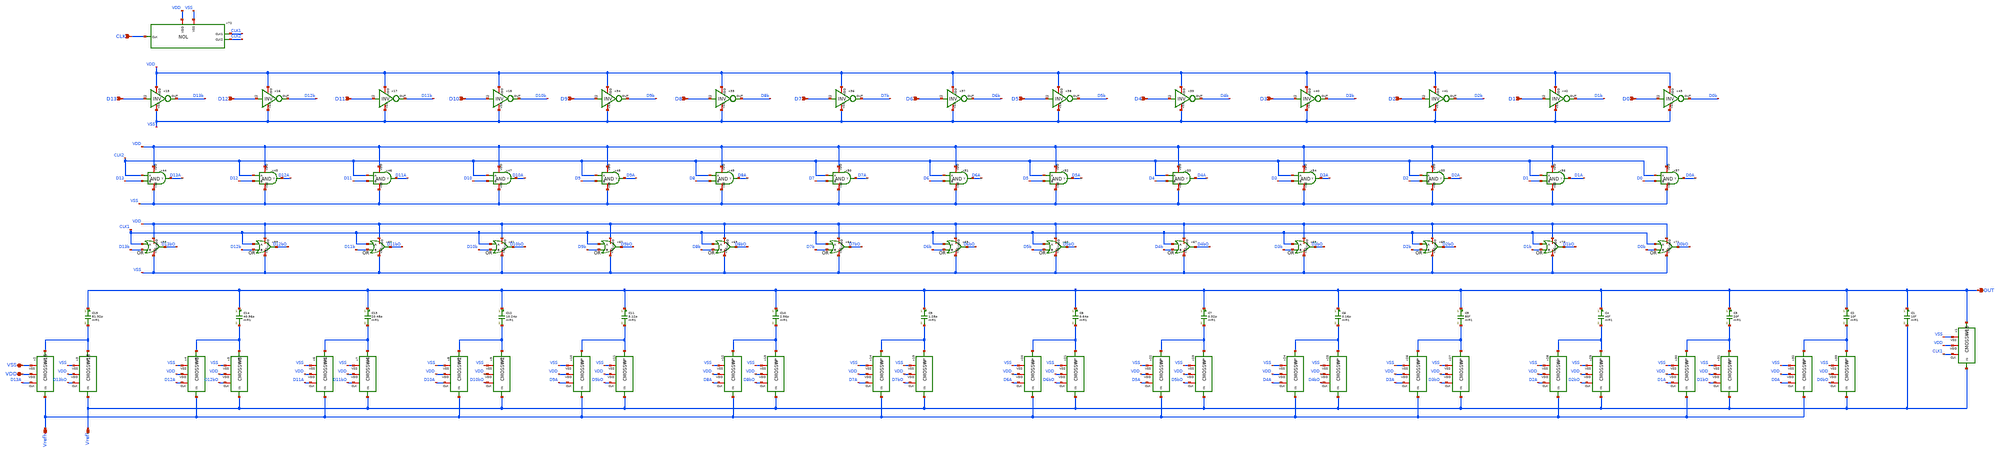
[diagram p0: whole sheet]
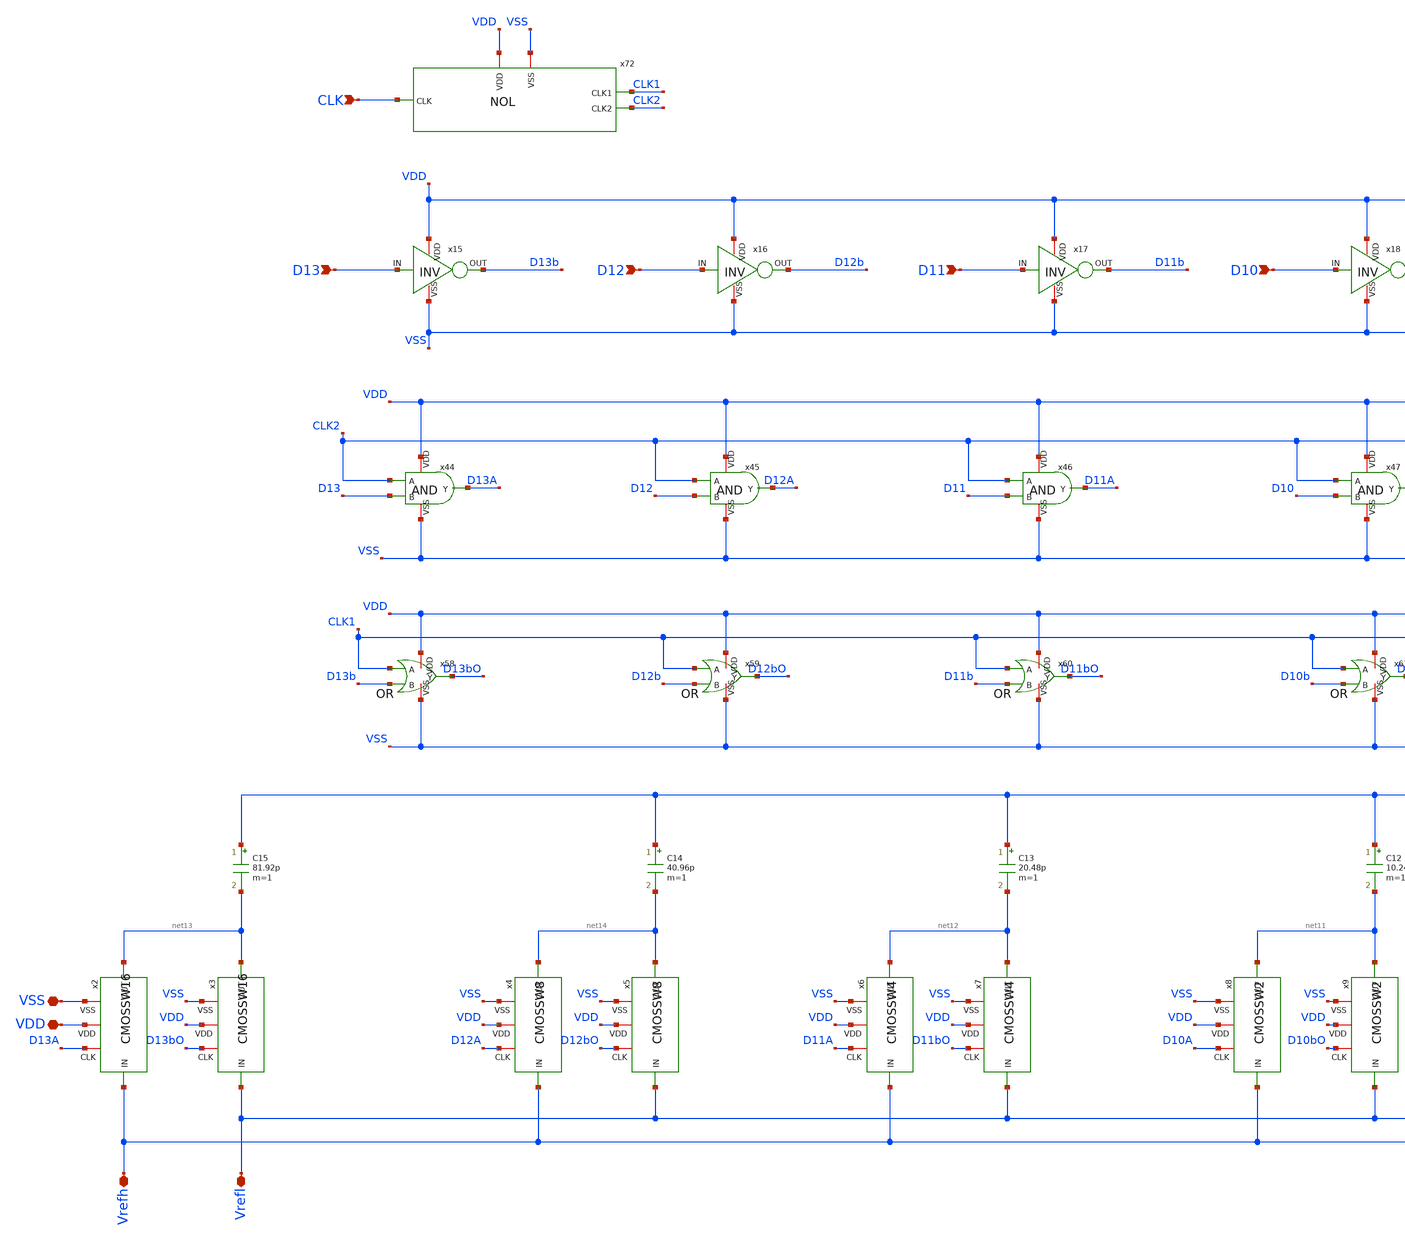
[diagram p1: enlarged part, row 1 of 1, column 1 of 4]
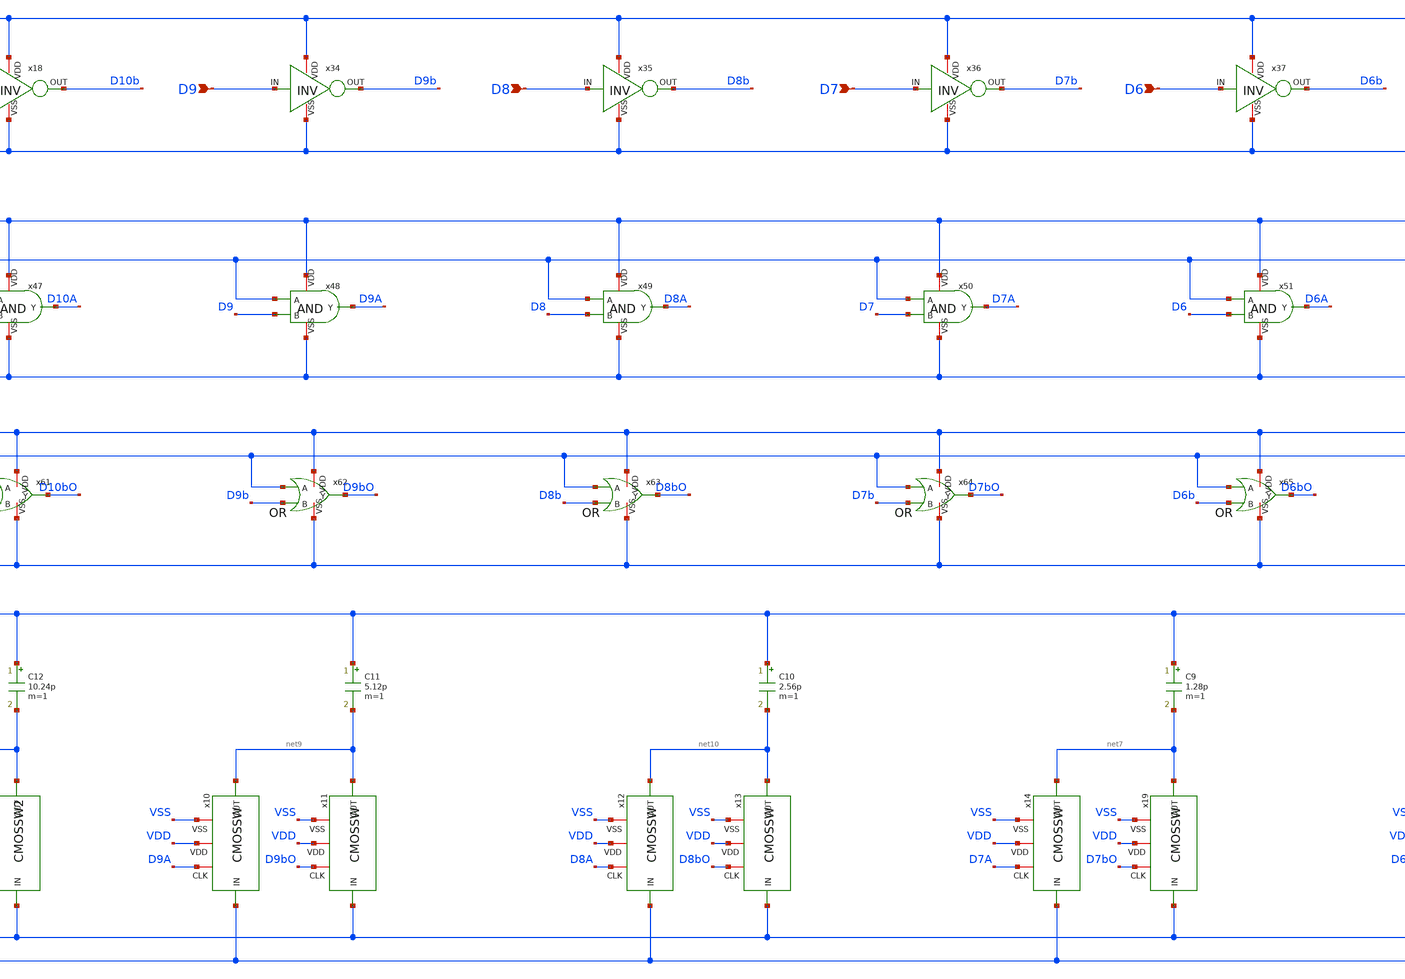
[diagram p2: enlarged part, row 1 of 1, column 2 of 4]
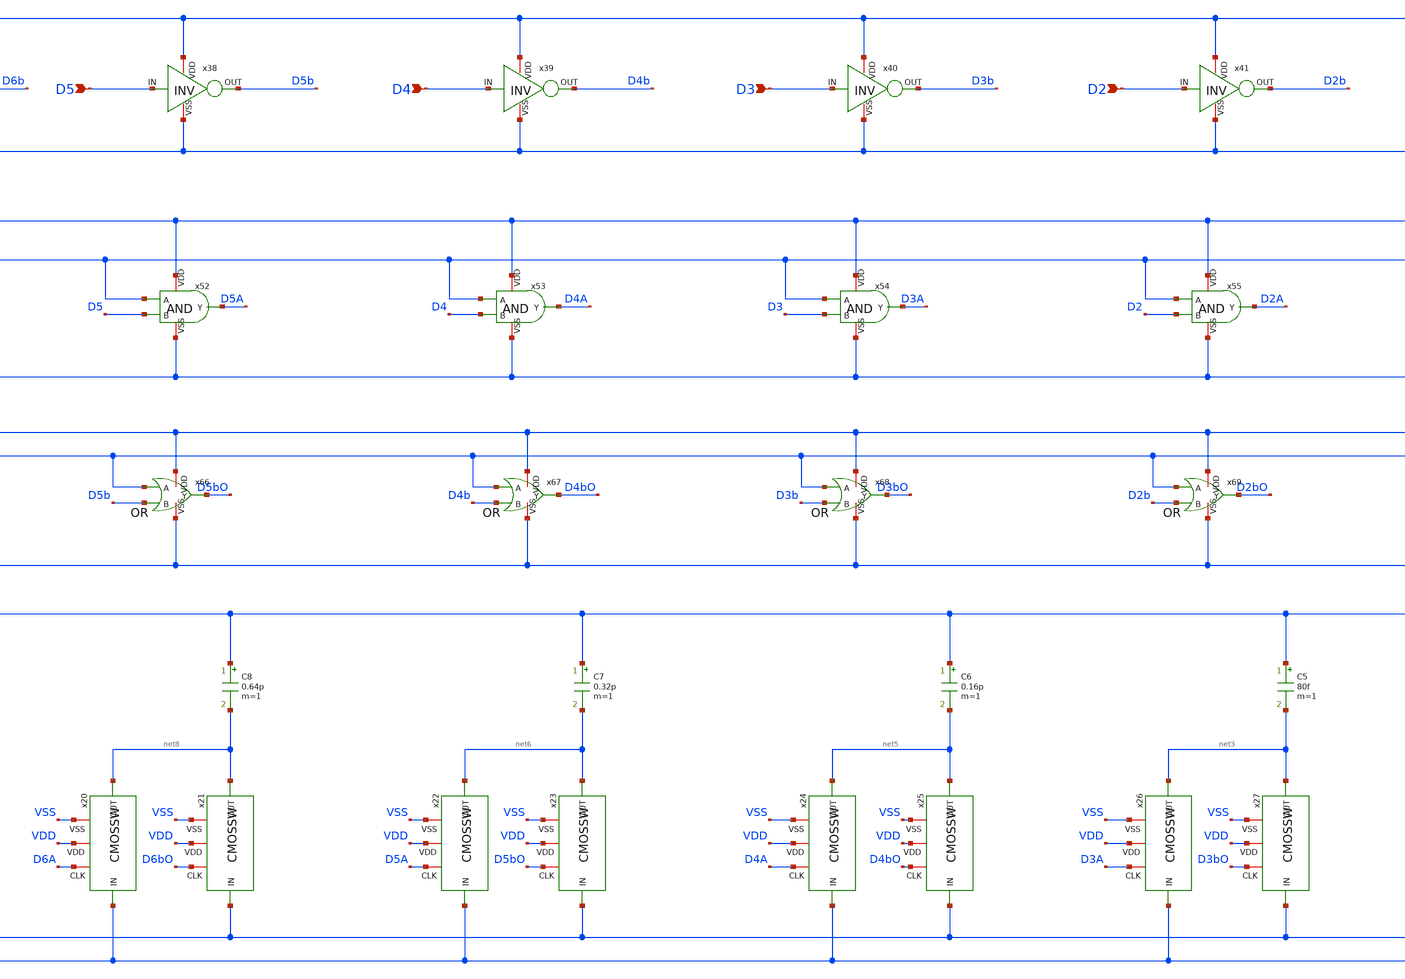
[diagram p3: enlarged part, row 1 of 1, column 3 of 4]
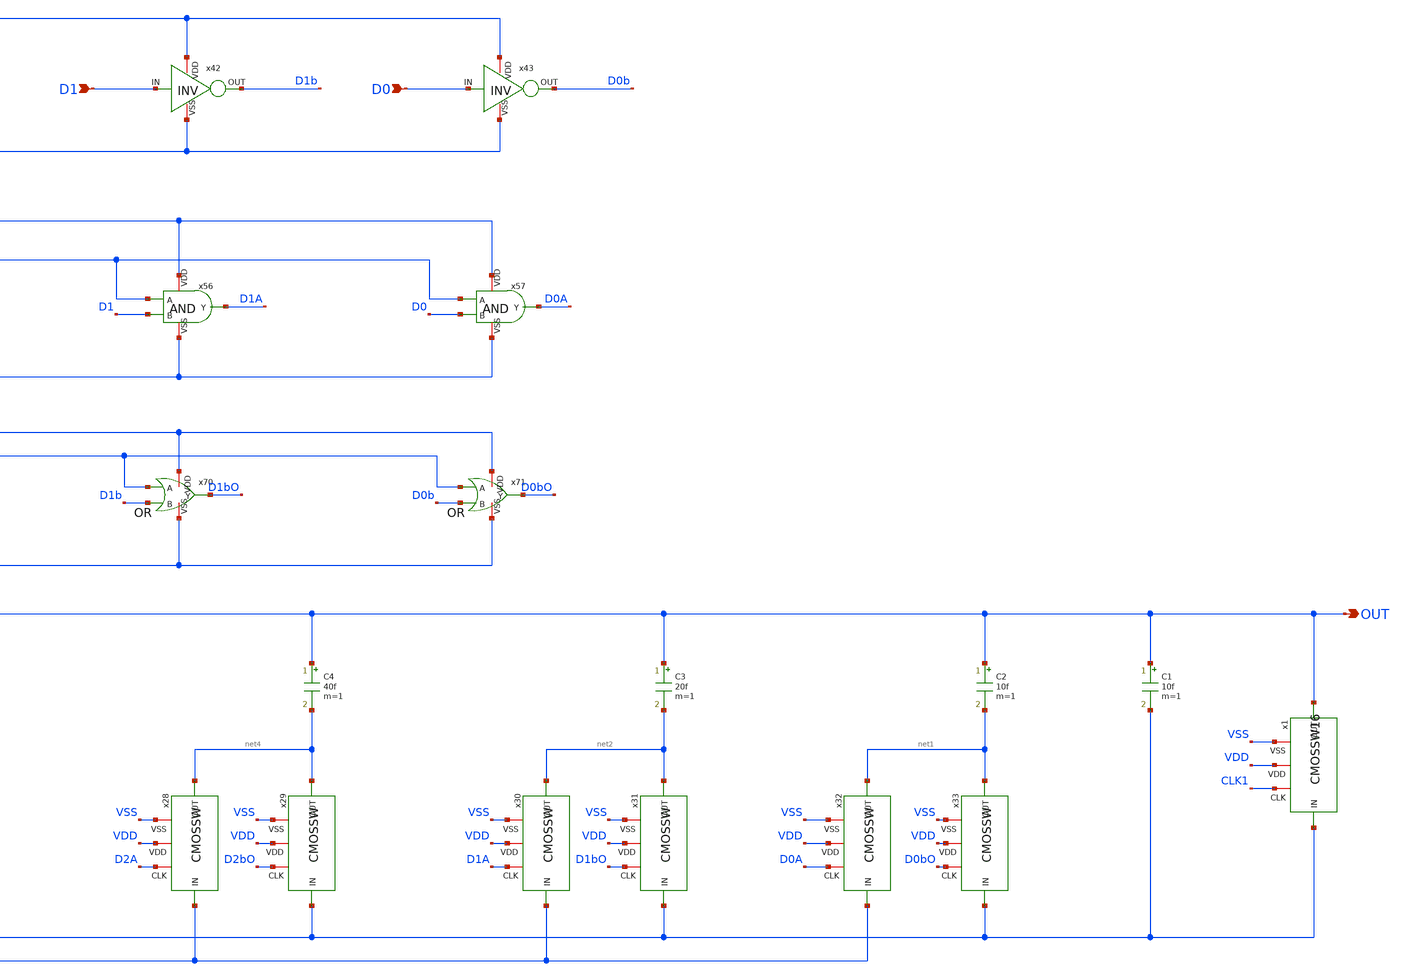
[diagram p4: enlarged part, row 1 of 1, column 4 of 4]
** sch_path: CDAC_CMOSSW.sch
**.subckt CDAC_CMOSSW OUT Vrefh Vrefl D13 D12 D11 D10 VSS VDD D9 D8 D7 D6 D5 D4 D3 D2 D1 D0 CLK
*.opin OUT
*.iopin Vrefh
*.iopin Vrefl
*.ipin D13
*.ipin D12
*.ipin D11
*.ipin D10
*.iopin VSS
*.iopin VDD
*.ipin D9
*.ipin D8
*.ipin D7
*.ipin D6
*.ipin D5
*.ipin D4
*.ipin D3
*.ipin D2
*.ipin D1
*.ipin D0
*.ipin CLK
C1 OUT Vrefl 10f m=1
C2 OUT net1 10f m=1
C3 OUT net2 20f m=1
C4 OUT net4 40f m=1
C5 OUT net3 80f m=1
x15 VDD D13b D13 VSS INV
x16 VDD D12b D12 VSS INV
x17 VDD D11b D11 VSS INV
x18 VDD D10b D10 VSS INV
C6 OUT net5 0.16p m=1
C7 OUT net6 0.32p m=1
C8 OUT net8 0.64p m=1
C9 OUT net7 1.28p m=1
C10 OUT net10 2.56p m=1
C11 OUT net9 5.12p m=1
C12 OUT net11 10.24p m=1
C13 OUT net12 20.48p m=1
C14 OUT net14 40.96p m=1
C15 OUT net13 81.92p m=1
x34 VDD D9b D9 VSS INV
x35 VDD D8b D8 VSS INV
x36 VDD D7b D7 VSS INV
x37 VDD D6b D6 VSS INV
x38 VDD D5b D5 VSS INV
x39 VDD D4b D4 VSS INV
x40 VDD D3b D3 VSS INV
x41 VDD D2b D2 VSS INV
x42 VDD D1b D1 VSS INV
x43 VDD D0b D0 VSS INV
x44 VDD D13A CLK2 D13 VSS AND
x45 VDD D12A CLK2 D12 VSS AND
x46 VDD D11A CLK2 D11 VSS AND
x47 VDD D10A CLK2 D10 VSS AND
x48 VDD D9A CLK2 D9 VSS AND
x49 VDD D8A CLK2 D8 VSS AND
x50 VDD D7A CLK2 D7 VSS AND
x51 VDD D6A CLK2 D6 VSS AND
x52 VDD D5A CLK2 D5 VSS AND
x53 VDD D4A CLK2 D4 VSS AND
x54 VDD D3A CLK2 D3 VSS AND
x55 VDD D2A CLK2 D2 VSS AND
x56 VDD D1A CLK2 D1 VSS AND
x57 VDD D0A CLK2 D0 VSS AND
x58 VDD CLK1 D13bO D13b VSS OR
x59 VDD CLK1 D12bO D12b VSS OR
x60 VDD CLK1 D11bO D11b VSS OR
x61 VDD CLK1 D10bO D10b VSS OR
x62 VDD CLK1 D9bO D9b VSS OR
x63 VDD CLK1 D8bO D8b VSS OR
x64 VDD CLK1 D7bO D7b VSS OR
x65 VDD CLK1 D6bO D6b VSS OR
x66 VDD CLK1 D5bO D5b VSS OR
x67 VDD CLK1 D4bO D4b VSS OR
x68 VDD CLK1 D3bO D3b VSS OR
x69 VDD CLK1 D2bO D2b VSS OR
x70 VDD CLK1 D1bO D1b VSS OR
x71 VDD CLK1 D0bO D0b VSS OR
x72 VDD CLK CLK1 VSS CLK2 NOL
x1 CLK1 VSS OUT Vrefl VDD CMOSSW16
x2 D13A VSS net13 Vrefh VDD CMOSSW16
x3 D13bO VSS net13 Vrefl VDD CMOSSW16
x4 D12A VSS net14 Vrefh VDD CMOSSW8
x5 D12bO VSS net14 Vrefl VDD CMOSSW8
x6 D11A VSS net12 Vrefh VDD CMOSSW4
x7 D11bO VSS net12 Vrefl VDD CMOSSW4
x8 D10A VSS net11 Vrefh VDD CMOSSW2
x9 D10bO VSS net11 Vrefl VDD CMOSSW2
x10 D9A VSS net9 Vrefh VDD CMOSSW
x11 D9bO VSS net9 Vrefl VDD CMOSSW
x12 D8A VSS net10 Vrefh VDD CMOSSW
x13 D8bO VSS net10 Vrefl VDD CMOSSW
x14 D7A VSS net7 Vrefh VDD CMOSSW
x19 D7bO VSS net7 Vrefl VDD CMOSSW
x20 D6A VSS net8 Vrefh VDD CMOSSW
x21 D6bO VSS net8 Vrefl VDD CMOSSW
x22 D5A VSS net6 Vrefh VDD CMOSSW
x23 D5bO VSS net6 Vrefl VDD CMOSSW
x24 D4A VSS net5 Vrefh VDD CMOSSW
x25 D4bO VSS net5 Vrefl VDD CMOSSW
x26 D3A VSS net3 Vrefh VDD CMOSSW
x27 D3bO VSS net3 Vrefl VDD CMOSSW
x28 D2A VSS net4 Vrefh VDD CMOSSW
x29 D2bO VSS net4 Vrefl VDD CMOSSW
x30 D1A VSS net2 Vrefh VDD CMOSSW
x31 D1bO VSS net2 Vrefl VDD CMOSSW
x32 D0A VSS net1 Vrefh VDD CMOSSW
x33 D0bO VSS net1 Vrefl VDD CMOSSW
**.ends
.end
